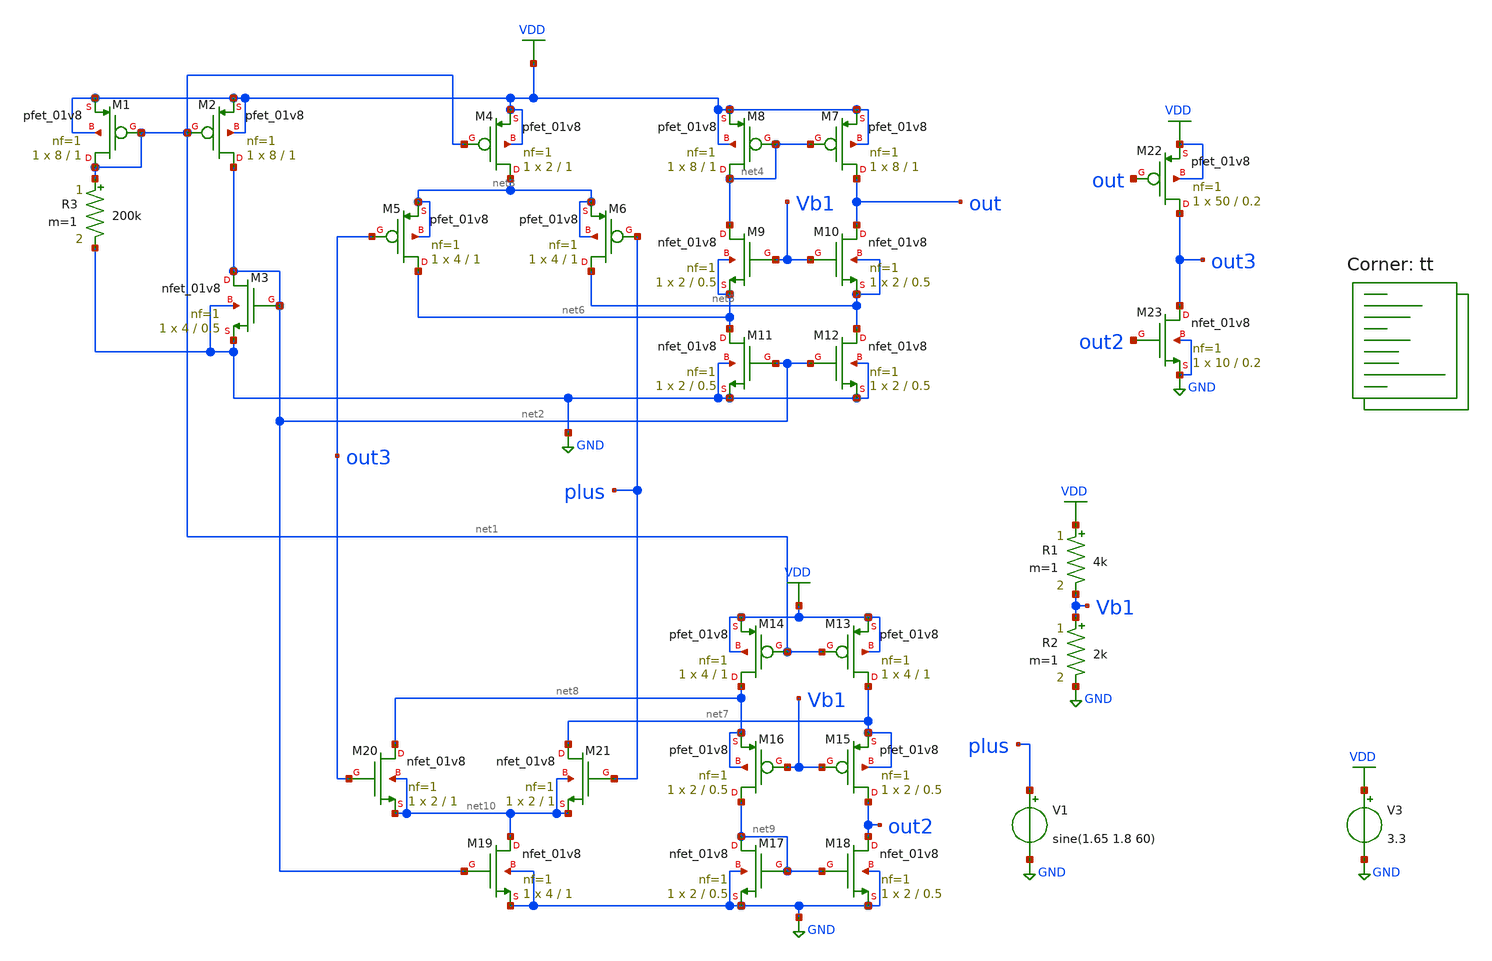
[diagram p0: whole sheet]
** sch_path: opamp_3.3v/schematic/schem.sch
**.subckt schem
V1 plus GND sine(1.65 1.8 60)
V3 VDD GND 3.3
XM1 net1 net1 VDD VDD sky130_fd_pr__pfet_01v8 L=1 W=8 nf=1 ad='int((nf+1)/2) * W/nf * 0.29' as='int((nf+2)/2) * W/nf * 0.29'
+ pd='2*int((nf+1)/2) * (W/nf + 0.29)' ps='2*int((nf+2)/2) * (W/nf + 0.29)' nrd='0.29 / W' nrs='0.29 / W'
+ sa=0 sb=0 sd=0 mult=1 m=1
XM2 net2 net1 VDD VDD sky130_fd_pr__pfet_01v8 L=1 W=8 nf=1 ad='int((nf+1)/2) * W/nf * 0.29' as='int((nf+2)/2) * W/nf * 0.29'
+ pd='2*int((nf+1)/2) * (W/nf + 0.29)' ps='2*int((nf+2)/2) * (W/nf + 0.29)' nrd='0.29 / W' nrs='0.29 / W'
+ sa=0 sb=0 sd=0 mult=1 m=1
XM3 net2 net2 GND GND sky130_fd_pr__nfet_01v8 L=0.5 W=4 nf=1 ad='int((nf+1)/2) * W/nf * 0.29' as='int((nf+2)/2) * W/nf * 0.29'
+ pd='2*int((nf+1)/2) * (W/nf + 0.29)' ps='2*int((nf+2)/2) * (W/nf + 0.29)' nrd='0.29 / W' nrs='0.29 / W'
+ sa=0 sb=0 sd=0 mult=1 m=1
XM4 net3 net1 VDD VDD sky130_fd_pr__pfet_01v8 L=1 W=2 nf=1 ad='int((nf+1)/2) * W/nf * 0.29' as='int((nf+2)/2) * W/nf * 0.29'
+ pd='2*int((nf+1)/2) * (W/nf + 0.29)' ps='2*int((nf+2)/2) * (W/nf + 0.29)' nrd='0.29 / W' nrs='0.29 / W'
+ sa=0 sb=0 sd=0 mult=1 m=1
XM5 net6 out3 net3 net3 sky130_fd_pr__pfet_01v8 L=1 W=4 nf=1 ad='int((nf+1)/2) * W/nf * 0.29' as='int((nf+2)/2) * W/nf * 0.29'
+ pd='2*int((nf+1)/2) * (W/nf + 0.29)' ps='2*int((nf+2)/2) * (W/nf + 0.29)' nrd='0.29 / W' nrs='0.29 / W'
+ sa=0 sb=0 sd=0 mult=1 m=1
XM6 net5 plus net3 net3 sky130_fd_pr__pfet_01v8 L=1 W=4 nf=1 ad='int((nf+1)/2) * W/nf * 0.29' as='int((nf+2)/2) * W/nf * 0.29'
+ pd='2*int((nf+1)/2) * (W/nf + 0.29)' ps='2*int((nf+2)/2) * (W/nf + 0.29)' nrd='0.29 / W' nrs='0.29 / W'
+ sa=0 sb=0 sd=0 mult=1 m=1
XM7 out net4 VDD VDD sky130_fd_pr__pfet_01v8 L=1 W=8 nf=1 ad='int((nf+1)/2) * W/nf * 0.29' as='int((nf+2)/2) * W/nf * 0.29'
+ pd='2*int((nf+1)/2) * (W/nf + 0.29)' ps='2*int((nf+2)/2) * (W/nf + 0.29)' nrd='0.29 / W' nrs='0.29 / W'
+ sa=0 sb=0 sd=0 mult=1 m=1
XM8 net4 net4 VDD VDD sky130_fd_pr__pfet_01v8 L=1 W=8 nf=1 ad='int((nf+1)/2) * W/nf * 0.29' as='int((nf+2)/2) * W/nf * 0.29'
+ pd='2*int((nf+1)/2) * (W/nf + 0.29)' ps='2*int((nf+2)/2) * (W/nf + 0.29)' nrd='0.29 / W' nrs='0.29 / W'
+ sa=0 sb=0 sd=0 mult=1 m=1
XM9 net4 Vb1 net6 net6 sky130_fd_pr__nfet_01v8 L=0.5 W=2 nf=1 ad='int((nf+1)/2) * W/nf * 0.29' as='int((nf+2)/2) * W/nf * 0.29'
+ pd='2*int((nf+1)/2) * (W/nf + 0.29)' ps='2*int((nf+2)/2) * (W/nf + 0.29)' nrd='0.29 / W' nrs='0.29 / W'
+ sa=0 sb=0 sd=0 mult=1 m=1
XM10 out Vb1 net5 net5 sky130_fd_pr__nfet_01v8 L=0.5 W=2 nf=1 ad='int((nf+1)/2) * W/nf * 0.29' as='int((nf+2)/2) * W/nf * 0.29'
+ pd='2*int((nf+1)/2) * (W/nf + 0.29)' ps='2*int((nf+2)/2) * (W/nf + 0.29)' nrd='0.29 / W' nrs='0.29 / W'
+ sa=0 sb=0 sd=0 mult=1 m=1
XM11 net6 net2 GND GND sky130_fd_pr__nfet_01v8 L=0.5 W=2 nf=1 ad='int((nf+1)/2) * W/nf * 0.29' as='int((nf+2)/2) * W/nf * 0.29'
+ pd='2*int((nf+1)/2) * (W/nf + 0.29)' ps='2*int((nf+2)/2) * (W/nf + 0.29)' nrd='0.29 / W' nrs='0.29 / W'
+ sa=0 sb=0 sd=0 mult=1 m=1
XM12 net5 net2 GND GND sky130_fd_pr__nfet_01v8 L=0.5 W=2 nf=1 ad='int((nf+1)/2) * W/nf * 0.29' as='int((nf+2)/2) * W/nf * 0.29'
+ pd='2*int((nf+1)/2) * (W/nf + 0.29)' ps='2*int((nf+2)/2) * (W/nf + 0.29)' nrd='0.29 / W' nrs='0.29 / W'
+ sa=0 sb=0 sd=0 mult=1 m=1
XM13 net7 net1 VDD VDD sky130_fd_pr__pfet_01v8 L=1 W=4 nf=1 ad='int((nf+1)/2) * W/nf * 0.29' as='int((nf+2)/2) * W/nf * 0.29'
+ pd='2*int((nf+1)/2) * (W/nf + 0.29)' ps='2*int((nf+2)/2) * (W/nf + 0.29)' nrd='0.29 / W' nrs='0.29 / W'
+ sa=0 sb=0 sd=0 mult=1 m=1
XM14 net8 net1 VDD VDD sky130_fd_pr__pfet_01v8 L=1 W=4 nf=1 ad='int((nf+1)/2) * W/nf * 0.29' as='int((nf+2)/2) * W/nf * 0.29'
+ pd='2*int((nf+1)/2) * (W/nf + 0.29)' ps='2*int((nf+2)/2) * (W/nf + 0.29)' nrd='0.29 / W' nrs='0.29 / W'
+ sa=0 sb=0 sd=0 mult=1 m=1
XM17 net9 net9 GND GND sky130_fd_pr__nfet_01v8 L=0.5 W=2 nf=1 ad='int((nf+1)/2) * W/nf * 0.29' as='int((nf+2)/2) * W/nf * 0.29'
+ pd='2*int((nf+1)/2) * (W/nf + 0.29)' ps='2*int((nf+2)/2) * (W/nf + 0.29)' nrd='0.29 / W' nrs='0.29 / W'
+ sa=0 sb=0 sd=0 mult=1 m=1
XM18 out2 net9 GND GND sky130_fd_pr__nfet_01v8 L=0.5 W=2 nf=1 ad='int((nf+1)/2) * W/nf * 0.29' as='int((nf+2)/2) * W/nf * 0.29'
+ pd='2*int((nf+1)/2) * (W/nf + 0.29)' ps='2*int((nf+2)/2) * (W/nf + 0.29)' nrd='0.29 / W' nrs='0.29 / W'
+ sa=0 sb=0 sd=0 mult=1 m=1
XM15 out2 Vb1 net7 net7 sky130_fd_pr__pfet_01v8 L=0.5 W=2 nf=1 ad='int((nf+1)/2) * W/nf * 0.29' as='int((nf+2)/2) * W/nf * 0.29'
+ pd='2*int((nf+1)/2) * (W/nf + 0.29)' ps='2*int((nf+2)/2) * (W/nf + 0.29)' nrd='0.29 / W' nrs='0.29 / W'
+ sa=0 sb=0 sd=0 mult=1 m=1
XM16 net9 Vb1 net8 net8 sky130_fd_pr__pfet_01v8 L=0.5 W=2 nf=1 ad='int((nf+1)/2) * W/nf * 0.29' as='int((nf+2)/2) * W/nf * 0.29'
+ pd='2*int((nf+1)/2) * (W/nf + 0.29)' ps='2*int((nf+2)/2) * (W/nf + 0.29)' nrd='0.29 / W' nrs='0.29 / W'
+ sa=0 sb=0 sd=0 mult=1 m=1
XM19 net10 net2 GND GND sky130_fd_pr__nfet_01v8 L=1 W=4 nf=1 ad='int((nf+1)/2) * W/nf * 0.29' as='int((nf+2)/2) * W/nf * 0.29'
+ pd='2*int((nf+1)/2) * (W/nf + 0.29)' ps='2*int((nf+2)/2) * (W/nf + 0.29)' nrd='0.29 / W' nrs='0.29 / W'
+ sa=0 sb=0 sd=0 mult=1 m=1
XM20 net8 out3 net10 net10 sky130_fd_pr__nfet_01v8 L=1 W=2 nf=1 ad='int((nf+1)/2) * W/nf * 0.29' as='int((nf+2)/2) * W/nf * 0.29'
+ pd='2*int((nf+1)/2) * (W/nf + 0.29)' ps='2*int((nf+2)/2) * (W/nf + 0.29)' nrd='0.29 / W' nrs='0.29 / W'
+ sa=0 sb=0 sd=0 mult=1 m=1
XM21 net7 plus net10 net10 sky130_fd_pr__nfet_01v8 L=1 W=2 nf=1 ad='int((nf+1)/2) * W/nf * 0.29' as='int((nf+2)/2) * W/nf * 0.29'
+ pd='2*int((nf+1)/2) * (W/nf + 0.29)' ps='2*int((nf+2)/2) * (W/nf + 0.29)' nrd='0.29 / W' nrs='0.29 / W'
+ sa=0 sb=0 sd=0 mult=1 m=1
XM22 out3 out VDD VDD sky130_fd_pr__pfet_01v8 L=0.2 W=50 nf=1 ad='int((nf+1)/2) * W/nf * 0.29' as='int((nf+2)/2) * W/nf * 0.29'
+ pd='2*int((nf+1)/2) * (W/nf + 0.29)' ps='2*int((nf+2)/2) * (W/nf + 0.29)' nrd='0.29 / W' nrs='0.29 / W'
+ sa=0 sb=0 sd=0 mult=1 m=1
XM23 out3 out2 GND GND sky130_fd_pr__nfet_01v8 L=0.2 W=10 nf=1 ad='int((nf+1)/2) * W/nf * 0.29' as='int((nf+2)/2) * W/nf * 0.29'
+ pd='2*int((nf+1)/2) * (W/nf + 0.29)' ps='2*int((nf+2)/2) * (W/nf + 0.29)' nrd='0.29 / W' nrs='0.29 / W'
+ sa=0 sb=0 sd=0 mult=1 m=1
R1 VDD Vb1 4k m=1
R2 Vb1 GND 2k m=1
R3 net1 GND 200k m=1
**** begin user architecture code
.lib $::SKYWATER_MODELS/sky130.lib.spice tt
**** end user architecture code
**.ends
.GLOBAL GND
.GLOBAL VDD
**** begin user architecture code


.tran 100u 100m
.save all
.control
run

*For Transient Analysis
plot out3 plus vdd
plot out3 vs plus
.endc

.end


**** end user architecture code
.end
